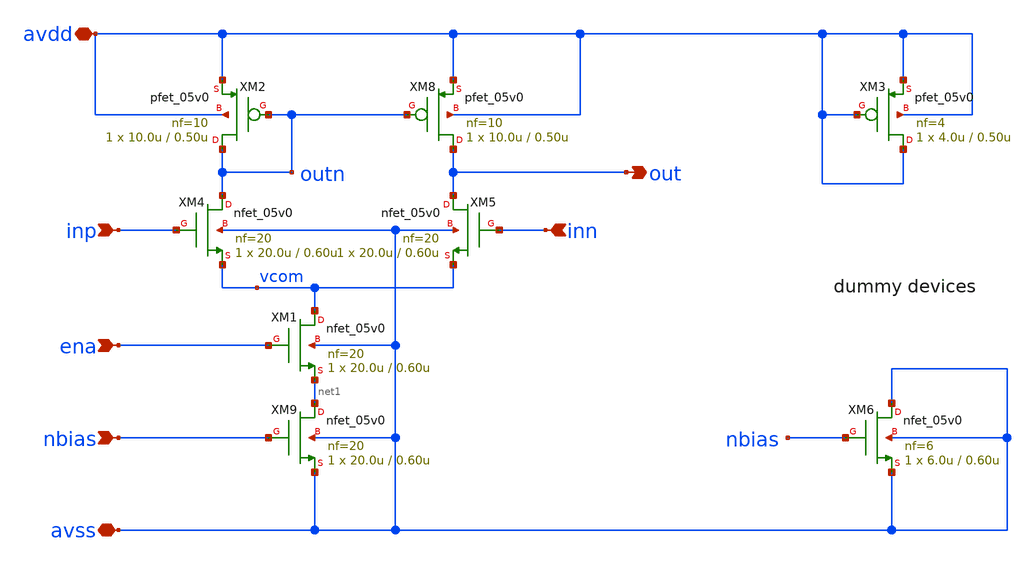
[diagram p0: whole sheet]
** sch_path: projects/programmable_transceiver_platform/analog/core_support/biasgen/xschem/bias_amp_large.sch
**.subckt bias_amp_large inp nbias inn out avdd avss ena
*.ipin inp
*.ipin nbias
*.ipin inn
*.opin out
*.iopin avdd
*.iopin avss
*.ipin ena
XM8 out outn avdd avdd pfet_05v0 L=0.50u W=10.0u nf=10 ad='int((nf+1)/2) * W/nf * 0.18u' as='int((nf+2)/2) * W/nf * 0.18u'
+ pd='2*int((nf+1)/2) * (W/nf + 0.18u)' ps='2*int((nf+2)/2) * (W/nf + 0.18u)' nrd='0.18u / W' nrs='0.18u / W'
+ sa=0 sb=0 sd=0 m=1 par=1
XM9 net1 nbias avss avss nfet_05v0 L=0.60u W=20.0u nf=20 ad='int((nf+1)/2) * W/nf * 0.18u' as='int((nf+2)/2) * W/nf * 0.18u'
+ pd='2*int((nf+1)/2) * (W/nf + 0.18u)' ps='2*int((nf+2)/2) * (W/nf + 0.18u)' nrd='0.18u / W' nrs='0.18u / W'
+ sa=0 sb=0 sd=0 m=1
XM1 vcom ena net1 avss nfet_05v0 L=0.60u W=20.0u nf=20 ad='int((nf+1)/2) * W/nf * 0.18u' as='int((nf+2)/2) * W/nf * 0.18u'
+ pd='2*int((nf+1)/2) * (W/nf + 0.18u)' ps='2*int((nf+2)/2) * (W/nf + 0.18u)' nrd='0.18u / W' nrs='0.18u / W'
+ sa=0 sb=0 sd=0 m=1
XM4 outn inp vcom avss nfet_05v0 L=0.60u W=20.0u nf=20 ad='int((nf+1)/2) * W/nf * 0.18u' as='int((nf+2)/2) * W/nf * 0.18u'
+ pd='2*int((nf+1)/2) * (W/nf + 0.18u)' ps='2*int((nf+2)/2) * (W/nf + 0.18u)' nrd='0.18u / W' nrs='0.18u / W'
+ sa=0 sb=0 sd=0 m=1
XM5 out inn vcom avss nfet_05v0 L=0.60u W=20.0u nf=20 ad='int((nf+1)/2) * W/nf * 0.18u' as='int((nf+2)/2) * W/nf * 0.18u'
+ pd='2*int((nf+1)/2) * (W/nf + 0.18u)' ps='2*int((nf+2)/2) * (W/nf + 0.18u)' nrd='0.18u / W' nrs='0.18u / W'
+ sa=0 sb=0 sd=0 m=1
XM2 outn outn avdd avdd pfet_05v0 L=0.50u W=10.0u nf=10 ad='int((nf+1)/2) * W/nf * 0.18u' as='int((nf+2)/2) * W/nf * 0.18u'
+ pd='2*int((nf+1)/2) * (W/nf + 0.18u)' ps='2*int((nf+2)/2) * (W/nf + 0.18u)' nrd='0.18u / W' nrs='0.18u / W'
+ sa=0 sb=0 sd=0 m=1 par=1
XM3 avdd avdd avdd avdd pfet_05v0 L=0.50u W=4.0u nf=4 ad='int((nf+1)/2) * W/nf * 0.18u' as='int((nf+2)/2) * W/nf * 0.18u'
+ pd='2*int((nf+1)/2) * (W/nf + 0.18u)' ps='2*int((nf+2)/2) * (W/nf + 0.18u)' nrd='0.18u / W' nrs='0.18u / W'
+ sa=0 sb=0 sd=0 m=1 par=1
XM6 avss nbias avss avss nfet_05v0 L=0.60u W=6.0u nf=6 ad='int((nf+1)/2) * W/nf * 0.18u' as='int((nf+2)/2) * W/nf * 0.18u'
+ pd='2*int((nf+1)/2) * (W/nf + 0.18u)' ps='2*int((nf+2)/2) * (W/nf + 0.18u)' nrd='0.18u / W' nrs='0.18u / W'
+ sa=0 sb=0 sd=0 m=1
**.ends
.end
